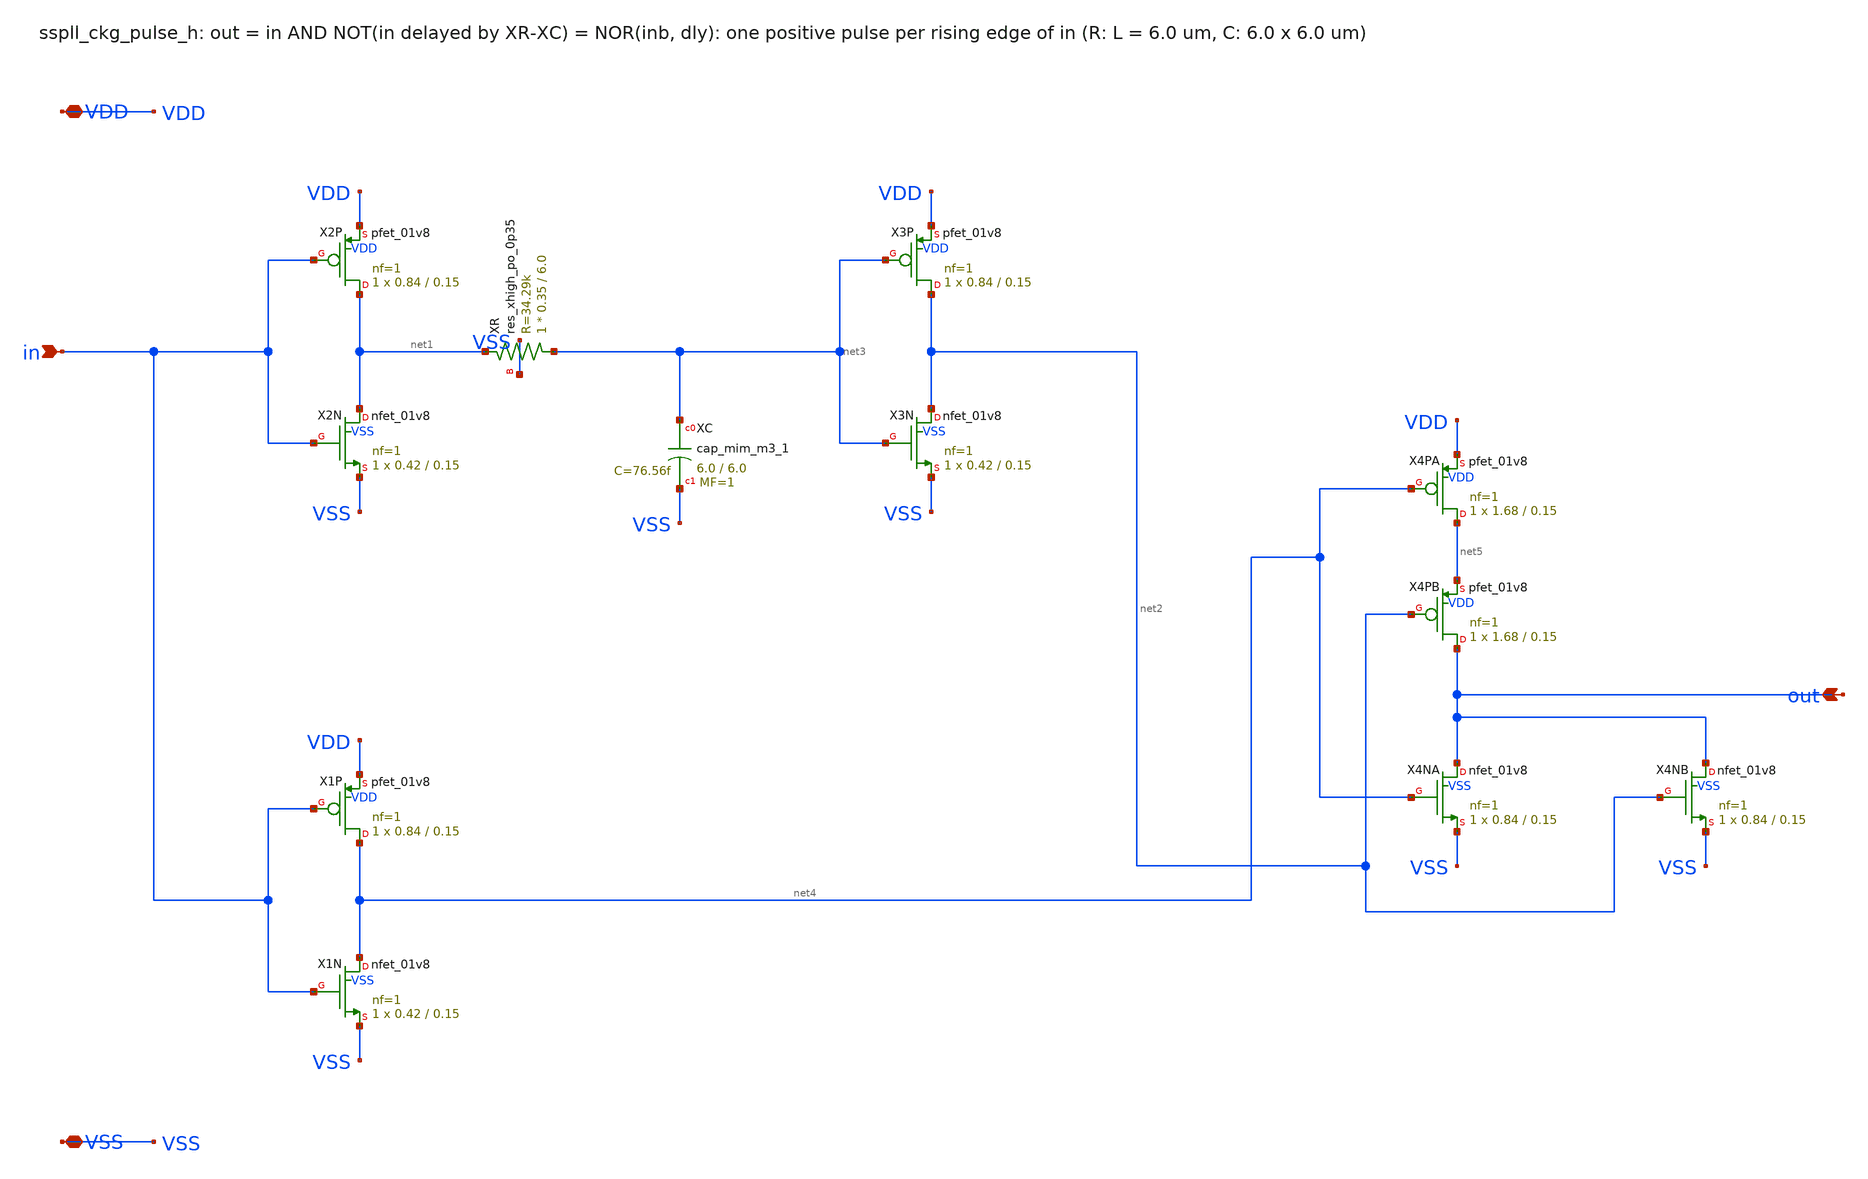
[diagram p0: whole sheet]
** sch_path: xschem/clkgen/sspll_ckg_pulse_h.sch
**.subckt sspll_ckg_pulse_h in out VDD VSS
*.ipin in
*.opin out
*.iopin VDD
*.iopin VSS
XX2P net1 in VDD VDD sky130_fd_pr__pfet_01v8 L=0.15 W=0.84 nf=1 ad='int((nf+1)/2) * W/nf * 0.29' as='int((nf+2)/2) * W/nf * 0.29'
+ pd='2*int((nf+1)/2) * (W/nf + 0.29)' ps='2*int((nf+2)/2) * (W/nf + 0.29)' nrd='0.29 / W' nrs='0.29 / W'
+ sa=0 sb=0 sd=0 mult=1 m=1
XX2N net1 in VSS VSS sky130_fd_pr__nfet_01v8 L=0.15 W=0.42 nf=1 ad='int((nf+1)/2) * W/nf * 0.29' as='int((nf+2)/2) * W/nf * 0.29'
+ pd='2*int((nf+1)/2) * (W/nf + 0.29)' ps='2*int((nf+2)/2) * (W/nf + 0.29)' nrd='0.29 / W' nrs='0.29 / W'
+ sa=0 sb=0 sd=0 mult=1 m=1
XXR net3 net1 VSS sky130_fd_pr__res_xhigh_po_0p35 L=6.0 mult=1 m=1
XXC net3 VSS sky130_fd_pr__cap_mim_m3_1 W=6.0 L=6.0 MF=1 m=1
XX3P net2 net3 VDD VDD sky130_fd_pr__pfet_01v8 L=0.15 W=0.84 nf=1 ad='int((nf+1)/2) * W/nf * 0.29' as='int((nf+2)/2) * W/nf * 0.29'
+ pd='2*int((nf+1)/2) * (W/nf + 0.29)' ps='2*int((nf+2)/2) * (W/nf + 0.29)' nrd='0.29 / W' nrs='0.29 / W'
+ sa=0 sb=0 sd=0 mult=1 m=1
XX3N net2 net3 VSS VSS sky130_fd_pr__nfet_01v8 L=0.15 W=0.42 nf=1 ad='int((nf+1)/2) * W/nf * 0.29' as='int((nf+2)/2) * W/nf * 0.29'
+ pd='2*int((nf+1)/2) * (W/nf + 0.29)' ps='2*int((nf+2)/2) * (W/nf + 0.29)' nrd='0.29 / W' nrs='0.29 / W'
+ sa=0 sb=0 sd=0 mult=1 m=1
XX1P net4 in VDD VDD sky130_fd_pr__pfet_01v8 L=0.15 W=0.84 nf=1 ad='int((nf+1)/2) * W/nf * 0.29' as='int((nf+2)/2) * W/nf * 0.29'
+ pd='2*int((nf+1)/2) * (W/nf + 0.29)' ps='2*int((nf+2)/2) * (W/nf + 0.29)' nrd='0.29 / W' nrs='0.29 / W'
+ sa=0 sb=0 sd=0 mult=1 m=1
XX1N net4 in VSS VSS sky130_fd_pr__nfet_01v8 L=0.15 W=0.42 nf=1 ad='int((nf+1)/2) * W/nf * 0.29' as='int((nf+2)/2) * W/nf * 0.29'
+ pd='2*int((nf+1)/2) * (W/nf + 0.29)' ps='2*int((nf+2)/2) * (W/nf + 0.29)' nrd='0.29 / W' nrs='0.29 / W'
+ sa=0 sb=0 sd=0 mult=1 m=1
XX4PA net5 net4 VDD VDD sky130_fd_pr__pfet_01v8 L=0.15 W=1.68 nf=1 ad='int((nf+1)/2) * W/nf * 0.29' as='int((nf+2)/2) * W/nf * 0.29'
+ pd='2*int((nf+1)/2) * (W/nf + 0.29)' ps='2*int((nf+2)/2) * (W/nf + 0.29)' nrd='0.29 / W' nrs='0.29 / W'
+ sa=0 sb=0 sd=0 mult=1 m=1
XX4PB out net2 net5 VDD sky130_fd_pr__pfet_01v8 L=0.15 W=1.68 nf=1 ad='int((nf+1)/2) * W/nf * 0.29' as='int((nf+2)/2) * W/nf * 0.29'
+ pd='2*int((nf+1)/2) * (W/nf + 0.29)' ps='2*int((nf+2)/2) * (W/nf + 0.29)' nrd='0.29 / W' nrs='0.29 / W'
+ sa=0 sb=0 sd=0 mult=1 m=1
XX4NA out net4 VSS VSS sky130_fd_pr__nfet_01v8 L=0.15 W=0.84 nf=1 ad='int((nf+1)/2) * W/nf * 0.29' as='int((nf+2)/2) * W/nf * 0.29'
+ pd='2*int((nf+1)/2) * (W/nf + 0.29)' ps='2*int((nf+2)/2) * (W/nf + 0.29)' nrd='0.29 / W' nrs='0.29 / W'
+ sa=0 sb=0 sd=0 mult=1 m=1
XX4NB out net2 VSS VSS sky130_fd_pr__nfet_01v8 L=0.15 W=0.84 nf=1 ad='int((nf+1)/2) * W/nf * 0.29' as='int((nf+2)/2) * W/nf * 0.29'
+ pd='2*int((nf+1)/2) * (W/nf + 0.29)' ps='2*int((nf+2)/2) * (W/nf + 0.29)' nrd='0.29 / W' nrs='0.29 / W'
+ sa=0 sb=0 sd=0 mult=1 m=1
**.ends
.end
